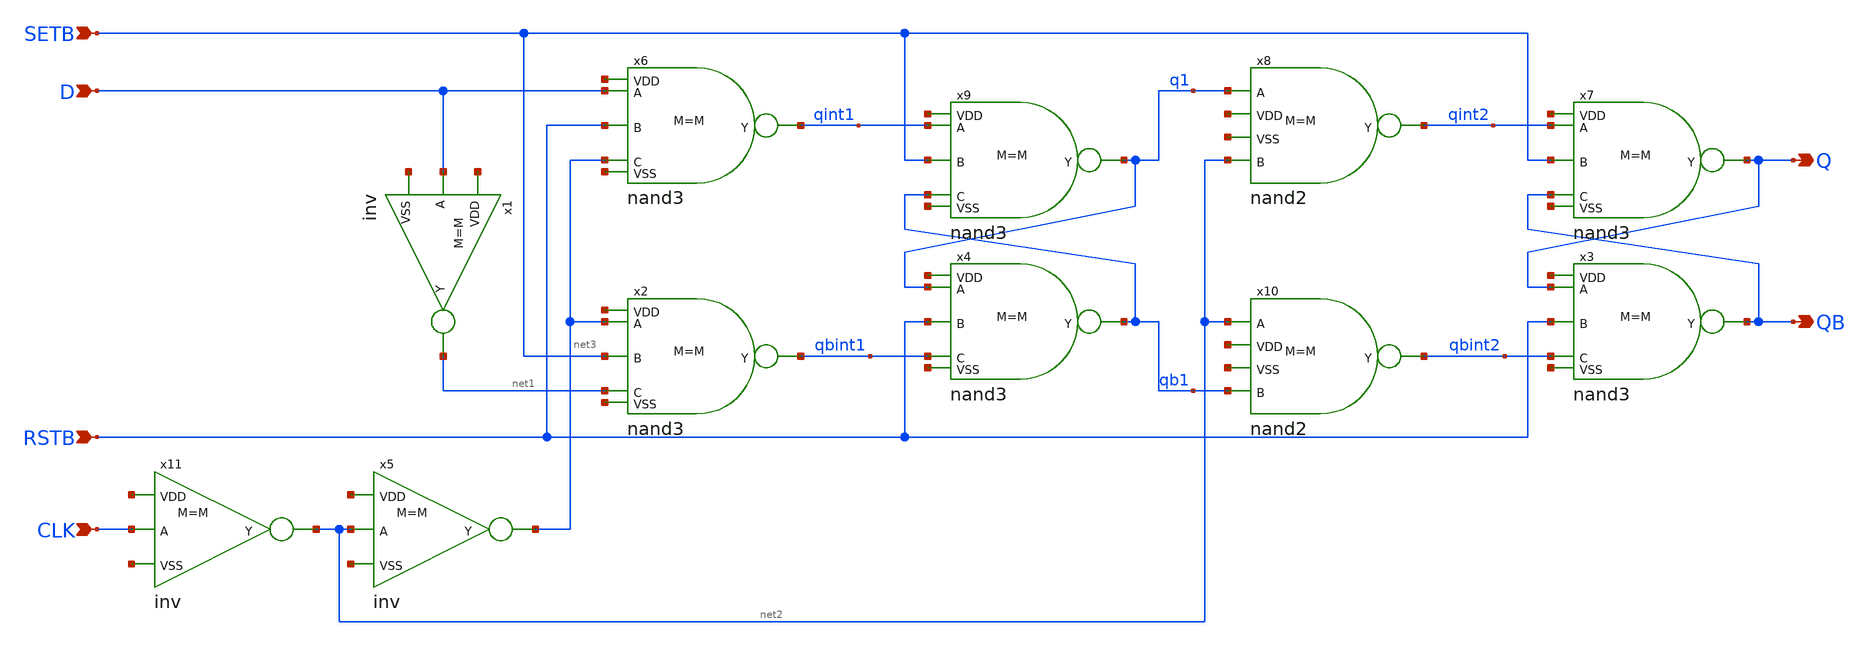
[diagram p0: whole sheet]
** sch_path: designs/dffsr.sch
**.subckt dffsr D CLK Q QB RSTB SETB
*.ipin D
*.ipin CLK
*.opin Q
*.opin QB
*.ipin RSTB
*.ipin SETB
x5 net2 net3 net4 net5 inv M=M
x1 D net1 net6 net7 inv M=M
x8 q1 qint2 net2 net8 net9 nand2 M=M
x10 net2 qbint2 qb1 net10 net11 nand2 M=M
x11 CLK net2 net12 net13 inv M=M
x3 Q RSTB qbint2 QB net14 net15 nand3 M=M
x4 q1 RSTB qbint1 qb1 net16 net17 nand3 M=M
x6 D RSTB net3 qint1 net18 net19 nand3 M=M
x2 net3 SETB net1 qbint1 net20 net21 nand3 M=M
x9 qint1 SETB qb1 q1 net22 net23 nand3 M=M
x7 qint2 SETB QB Q net24 net25 nand3 M=M
**.ends
.end
